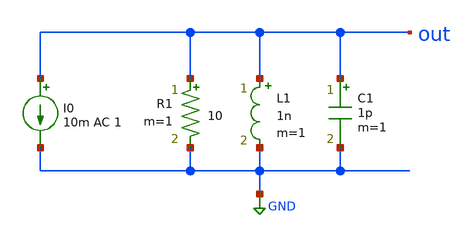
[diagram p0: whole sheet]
** sch_path: circuits-pub/RF/RLC_Networks/Parallel_RLC_Tank/parallel_rlc_tank.sch
**.subckt parallel_rlc_tank
L1 out GND 1n m=1
R1 out GND 10 m=1
C1 out GND 1p m=1
I0 out GND 10m AC 1
**** begin user architecture code



.options savecurrents

.control
save all

ac dec 10 1Meg 1T
plot db(v(out))


.endc



**** end user architecture code
**.ends
.GLOBAL GND
.end
